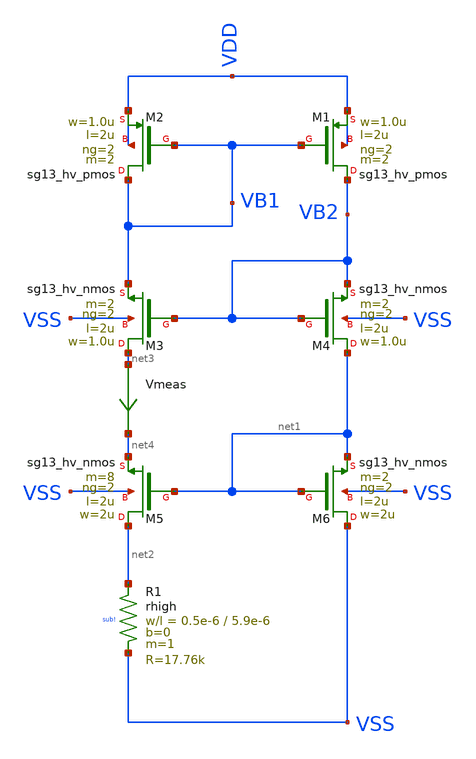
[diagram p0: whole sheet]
** sch_path: LIB/ihp-sg13g2/VA001/bias_cell.sch
**.subckt bias_cell
XM2 VB1 VB1 VDD VDD sg13_hv_pmos w=1.0u l=2u ng=2 m=2 mm_ok=1
XM1 VB2 VB1 VDD VDD sg13_hv_pmos w=1.0u l=2u ng=2 m=2 mm_ok=1
XM3 net3 VB2 VB1 VSS sg13_hv_nmos w=1.0u l=2u ng=2 m=2 mm_ok=1
XM4 net1 VB2 VB2 VSS sg13_hv_nmos w=1.0u l=2u ng=2 m=2 mm_ok=1
XM5 net2 net1 net4 VSS sg13_hv_nmos w=2u l=2u ng=2 m=8 mm_ok=1
XM6 VSS net1 net1 VSS sg13_hv_nmos w=2u l=2u ng=2 m=2 mm_ok=1
Vmeas net3 net4 0
.save i(vmeas)
XR1 net2 VSS sub! rhigh w=0.5e-6 l=5.9e-6 m=1 b=0 mm_ok=1
**.ends
.end
